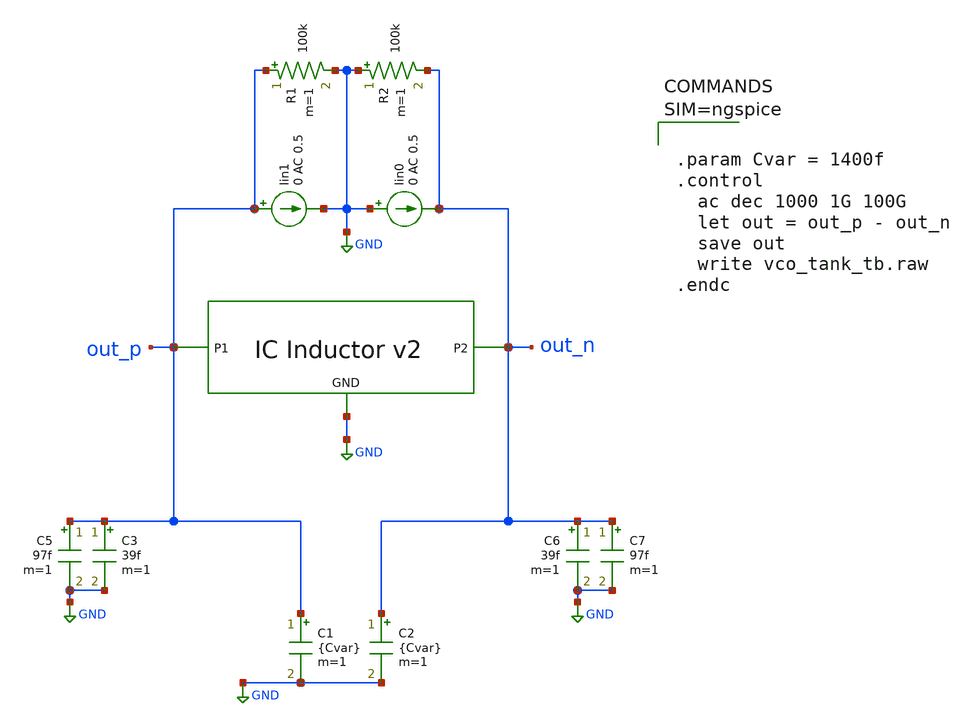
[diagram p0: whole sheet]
** sch_path: team_src/xschem/vco_tank_tb.sch
**.subckt vco_tank_tb
X1 out_p out_n GND vco_inductor_v2
C3 out_p GND 39f m=1
Iin0 GND out_n 0 AC 0.5
Iin1 out_p GND 0 AC 0.5
R1 out_p GND 100k m=1
R2 GND out_n 100k m=1
C1 out_p GND {Cvar} m=1
C2 out_n GND {Cvar} m=1
C5 out_p GND 97f m=1
C6 out_n GND 39f m=1
C7 out_n GND 97f m=1
**** begin user architecture code



.param Cvar = 1400f
.control
  ac dec 1000 1G 100G
  let out = out_p - out_n
  save out
  write vco_tank_tb.raw
.endc



**** end user architecture code
**.ends

* expanding   symbol:  vco_inductor_v2.sym # of pins=3
** sym_path: team_src/xschem/vco_inductor_v2.sym
.include $UPRJ_ROOT/team_src/xschem/vco_inductor_v2.subckt
.GLOBAL GND
.end
